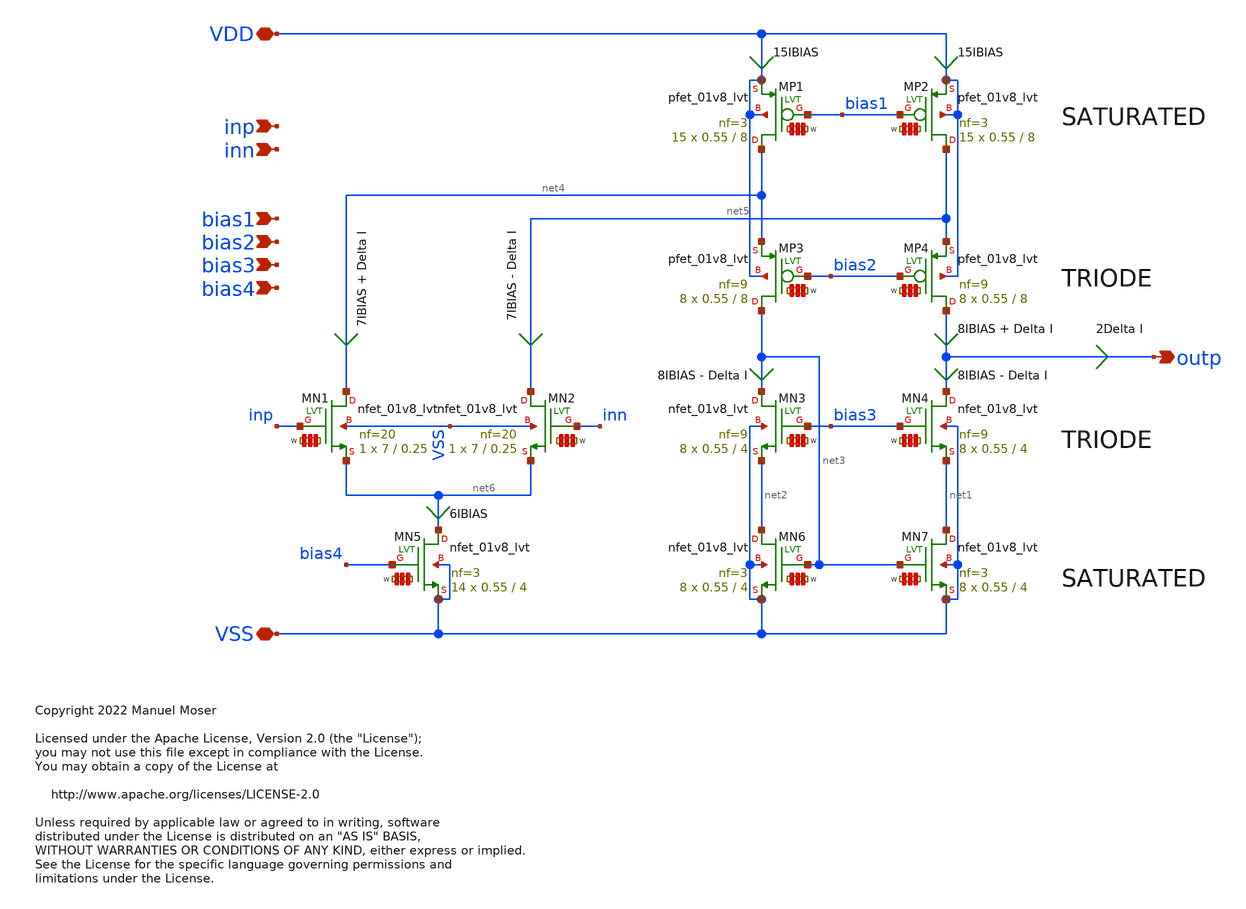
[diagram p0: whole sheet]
** sch_path: xschem/ldo_fc.sch
* Copyright 2022 Manuel Moser
* Licensed under the Apache License, Version 2.0 (the "License");
**.subckt ldo_fc VSS VDD inp inn bias1 outp bias2 bias3 bias4
*.iopin VSS
*.iopin VDD
*.ipin inp
*.ipin inn
*.ipin bias1
*.opin outp
*.ipin bias2
*.ipin bias3
*.ipin bias4
XMN4 outp bias3 net1 VSS sky130_fd_pr__nfet_01v8_lvt L=4 W='0.55 * 9 ' nf=9 ad='int((nf+1)/2) * W / nf * 0.29'
+ as='int((nf+2)/2) * W / nf * 0.29' pd='2*int((nf+1)/2) * (W / nf + 0.29)' ps='2*int((nf+2)/2) * (W / nf + 0.29)'
+ nrd='0.29 / W ' nrs='0.29 / W ' sa=0 sb=0 sd=0 mult=8 m=8
XMN7 net1 net3 VSS VSS sky130_fd_pr__nfet_01v8_lvt L=4 W='0.55 * 3 ' nf=3 ad='int((nf+1)/2) * W / nf * 0.29'
+ as='int((nf+2)/2) * W / nf * 0.29' pd='2*int((nf+1)/2) * (W / nf + 0.29)' ps='2*int((nf+2)/2) * (W / nf + 0.29)'
+ nrd='0.29 / W ' nrs='0.29 / W ' sa=0 sb=0 sd=0 mult=8 m=8
XMN3 net3 bias3 net2 VSS sky130_fd_pr__nfet_01v8_lvt L=4 W='0.55 * 9 ' nf=9 ad='int((nf+1)/2) * W / nf * 0.29'
+ as='int((nf+2)/2) * W / nf * 0.29' pd='2*int((nf+1)/2) * (W / nf + 0.29)' ps='2*int((nf+2)/2) * (W / nf + 0.29)'
+ nrd='0.29 / W ' nrs='0.29 / W ' sa=0 sb=0 sd=0 mult=8 m=8
XMN6 net2 net3 VSS VSS sky130_fd_pr__nfet_01v8_lvt L=4 W='0.55 * 3 ' nf=3 ad='int((nf+1)/2) * W / nf * 0.29'
+ as='int((nf+2)/2) * W / nf * 0.29' pd='2*int((nf+1)/2) * (W / nf + 0.29)' ps='2*int((nf+2)/2) * (W / nf + 0.29)'
+ nrd='0.29 / W ' nrs='0.29 / W ' sa=0 sb=0 sd=0 mult=8 m=8
XMP4 outp bias2 net5 VDD sky130_fd_pr__pfet_01v8_lvt L=8 W='0.55 * 9 ' nf=9 ad='int((nf+1)/2) * W / nf * 0.29'
+ as='int((nf+2)/2) * W / nf * 0.29' pd='2*int((nf+1)/2) * (W / nf + 0.29)' ps='2*int((nf+2)/2) * (W / nf + 0.29)'
+ nrd='0.29 / W ' nrs='0.29 / W ' sa=0 sb=0 sd=0 mult=8 m=8
XMP2 net5 bias1 VDD VDD sky130_fd_pr__pfet_01v8_lvt L=8 W='0.55 * 3 ' nf=3 ad='int((nf+1)/2) * W / nf * 0.29'
+ as='int((nf+2)/2) * W / nf * 0.29' pd='2*int((nf+1)/2) * (W / nf + 0.29)' ps='2*int((nf+2)/2) * (W / nf + 0.29)'
+ nrd='0.29 / W ' nrs='0.29 / W ' sa=0 sb=0 sd=0 mult=15 m=15
XMP3 net3 bias2 net4 VDD sky130_fd_pr__pfet_01v8_lvt L=8 W='0.55 * 9 ' nf=9 ad='int((nf+1)/2) * W / nf * 0.29'
+ as='int((nf+2)/2) * W / nf * 0.29' pd='2*int((nf+1)/2) * (W / nf + 0.29)' ps='2*int((nf+2)/2) * (W / nf + 0.29)'
+ nrd='0.29 / W ' nrs='0.29 / W ' sa=0 sb=0 sd=0 mult=8 m=8
XMP1 net4 bias1 VDD VDD sky130_fd_pr__pfet_01v8_lvt L=8 W='0.55 * 3 ' nf=3 ad='int((nf+1)/2) * W / nf * 0.29'
+ as='int((nf+2)/2) * W / nf * 0.29' pd='2*int((nf+1)/2) * (W / nf + 0.29)' ps='2*int((nf+2)/2) * (W / nf + 0.29)'
+ nrd='0.29 / W ' nrs='0.29 / W ' sa=0 sb=0 sd=0 mult=15 m=15
XMN5 net6 bias4 VSS VSS sky130_fd_pr__nfet_01v8_lvt L=4 W='0.55 * 3 ' nf=3 ad='int((nf+1)/2) * W / nf * 0.29'
+ as='int((nf+2)/2) * W / nf * 0.29' pd='2*int((nf+1)/2) * (W / nf + 0.29)' ps='2*int((nf+2)/2) * (W / nf + 0.29)'
+ nrd='0.29 / W ' nrs='0.29 / W ' sa=0 sb=0 sd=0 mult=14 m=14
XMN1 net4 inp net6 VSS sky130_fd_pr__nfet_01v8_lvt L=0.25 W='7 * 20 ' nf=20 ad='int((nf+1)/2) * W / nf * 0.29'
+ as='int((nf+2)/2) * W / nf * 0.29' pd='2*int((nf+1)/2) * (W / nf + 0.29)' ps='2*int((nf+2)/2) * (W / nf + 0.29)'
+ nrd='0.29 / W ' nrs='0.29 / W ' sa=0 sb=0 sd=0 mult=1 m=1
XMN2 net5 inn net6 VSS sky130_fd_pr__nfet_01v8_lvt L=0.25 W='7 * 20 ' nf=20 ad='int((nf+1)/2) * W / nf * 0.29'
+ as='int((nf+2)/2) * W / nf * 0.29' pd='2*int((nf+1)/2) * (W / nf + 0.29)' ps='2*int((nf+2)/2) * (W / nf + 0.29)'
+ nrd='0.29 / W ' nrs='0.29 / W ' sa=0 sb=0 sd=0 mult=1 m=1
**.ends
.end
